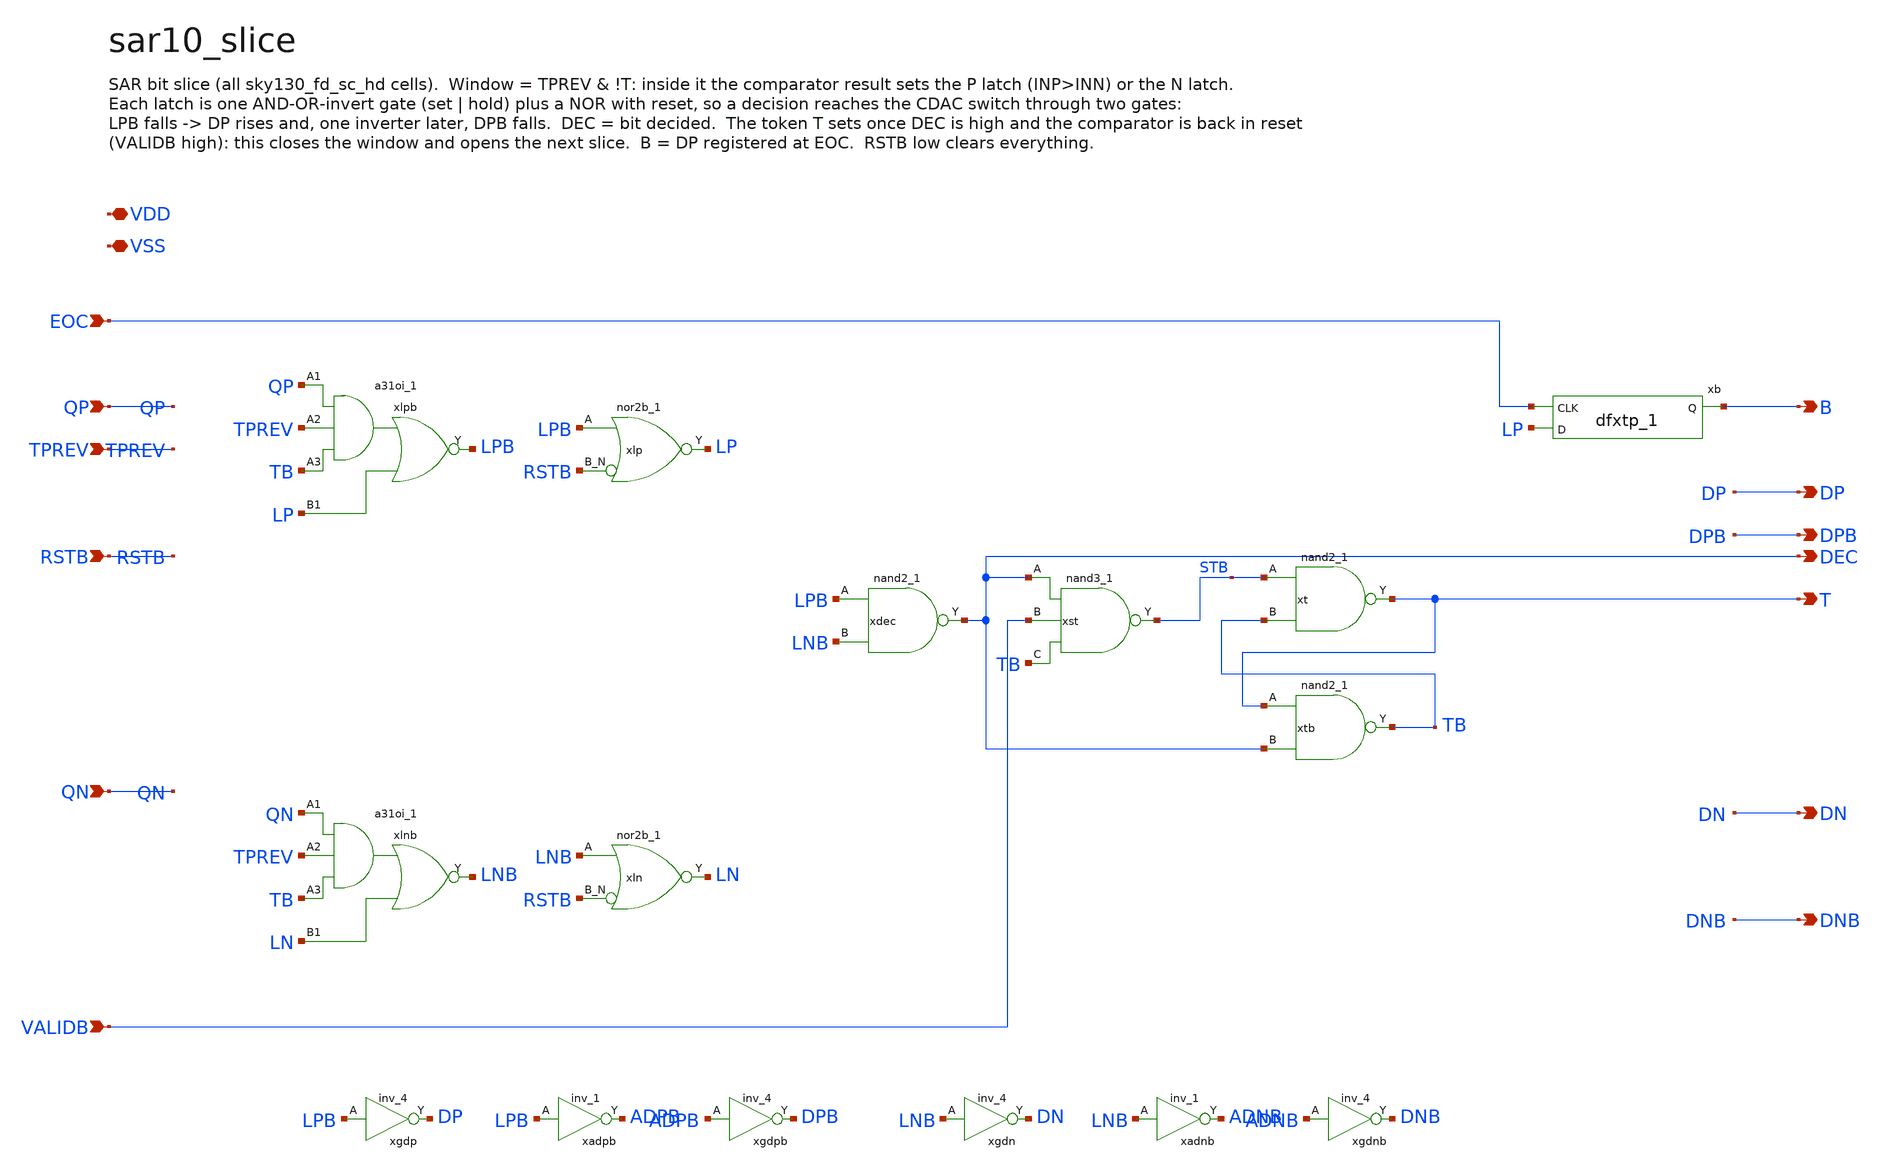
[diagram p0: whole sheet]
** sch_path: xschem/sar10_slice.sch
**.subckt sar10_slice QP TPREV RSTB QN VALIDB EOC B DP DPB DEC T DN DNB VDD VSS
*.ipin QP
*.ipin TPREV
*.ipin RSTB
*.ipin QN
*.ipin VALIDB
*.ipin EOC
*.opin B
*.opin DP
*.opin DPB
*.opin DEC
*.opin T
*.opin DN
*.opin DNB
*.iopin VDD
*.iopin VSS
xlpb QP TPREV TB LP VSS VSS VDD VDD LPB sky130_fd_sc_hd__a31oi_1
xlp LPB RSTB VSS VSS VDD VDD LP sky130_fd_sc_hd__nor2b_1
xlnb QN TPREV TB LN VSS VSS VDD VDD LNB sky130_fd_sc_hd__a31oi_1
xln LNB RSTB VSS VSS VDD VDD LN sky130_fd_sc_hd__nor2b_1
xdec LPB LNB VSS VSS VDD VDD DEC sky130_fd_sc_hd__nand2_1
xst DEC VALIDB TB VSS VSS VDD VDD STB sky130_fd_sc_hd__nand3_1
xt STB TB VSS VSS VDD VDD T sky130_fd_sc_hd__nand2_1
xtb T DEC VSS VSS VDD VDD TB sky130_fd_sc_hd__nand2_1
xb EOC LP VSS VSS VDD VDD B sky130_fd_sc_hd__dfxtp_1
xgdp LPB VSS VSS VDD VDD DP sky130_fd_sc_hd__inv_4
xadpb LPB VSS VSS VDD VDD ADPB sky130_fd_sc_hd__inv_1
xgdpb ADPB VSS VSS VDD VDD DPB sky130_fd_sc_hd__inv_4
xgdn LNB VSS VSS VDD VDD DN sky130_fd_sc_hd__inv_4
xadnb LNB VSS VSS VDD VDD ADNB sky130_fd_sc_hd__inv_1
xgdnb ADNB VSS VSS VDD VDD DNB sky130_fd_sc_hd__inv_4
**.ends
.end
